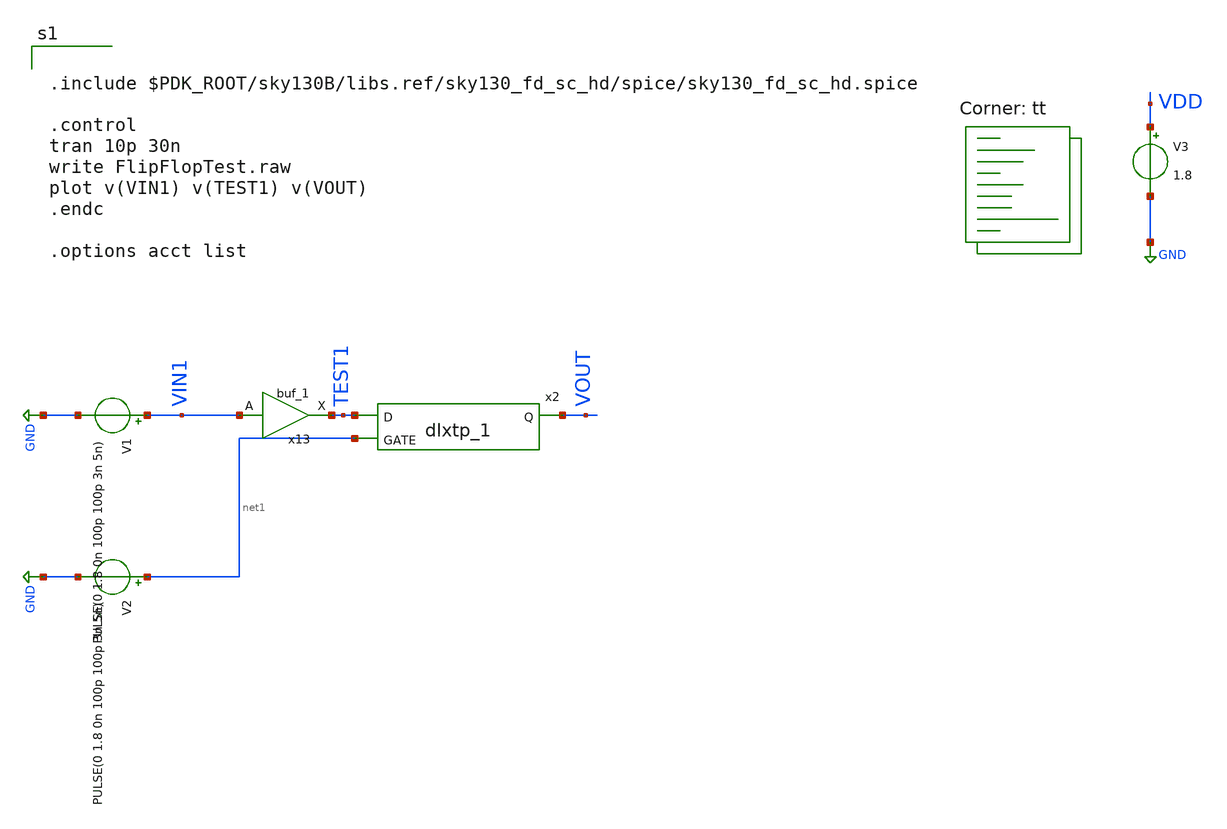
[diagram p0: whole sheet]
** sch_path: xschem/projects/FlipFlopTest.sch
**.subckt FlipFlopTest
V1 VIN1 GND PULSE(0 1.8 0n 100p 100p 3n 5n)
V2 net1 GND PULSE(0 1.8 0n 100p 100p 3n 5n)
V3 VDD GND 1.8
x2 TEST1 net1 0 0 VDD VDD VOUT sky130_fd_sc_hd__dlxtp_1
x13 VIN1 GND GND VDD VDD TEST1 sky130_fd_sc_hd__buf_1
**** begin user architecture code


.include $PDK_ROOT/sky130B/libs.ref/sky130_fd_sc_hd/spice/sky130_fd_sc_hd.spice

.control
tran 10p 30n
write FlipFlopTest.raw
plot v(VIN1) v(TEST1) v(VOUT)
.endc

.options acct list


.lib $::SKYWATER_MODELS/sky130.lib.spice tt
**** end user architecture code
**.ends
.GLOBAL GND
.end
